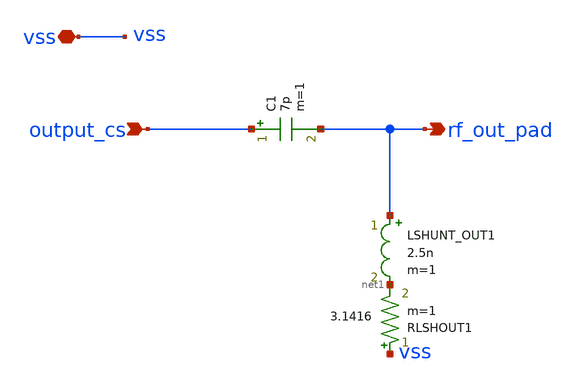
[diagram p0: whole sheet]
** sch_path: xschem/lna_core_output_match.sch
**.subckt lna_core_output_match output_cs vss rf_out_pad
*.ipin output_cs
*.iopin vss
*.opin rf_out_pad
C1 output_cs rf_out_pad 7p m=1
LSHUNT_OUT1 rf_out_pad net1 2.5n m=1
RLSHOUT1 vss net1 3.1416 m=1
**.ends
.end
